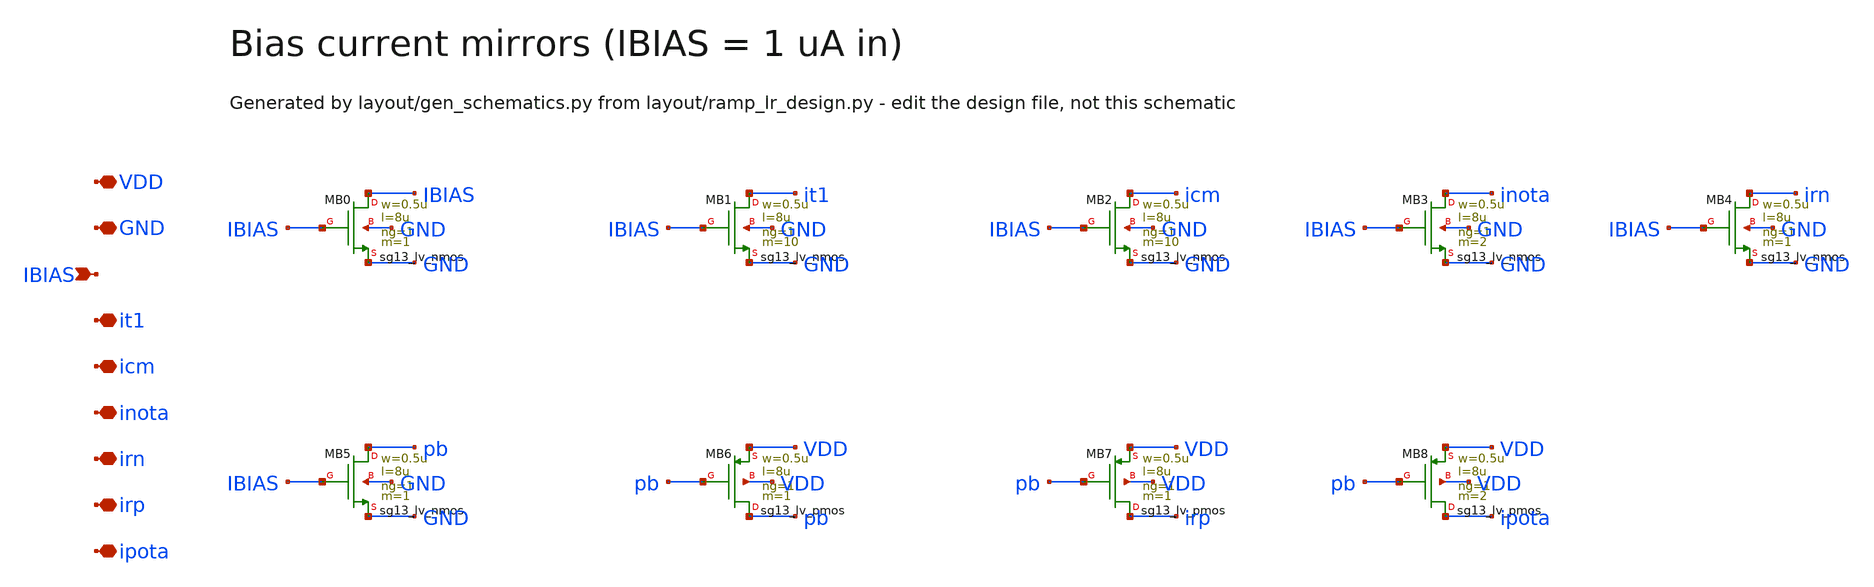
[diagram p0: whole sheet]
** sch_path: Design Files/RAMP/RAMP-LR/BIAS_LR.sch
**.subckt BIAS_LR VDD GND IBIAS it1 icm inota irn irp ipota
*.iopin VDD
*.iopin GND
*.ipin IBIAS
*.iopin it1
*.iopin icm
*.iopin inota
*.iopin irn
*.iopin irp
*.iopin ipota
XMB0 IBIAS IBIAS GND GND sg13_lv_nmos w=0.5u l=8u ng=1 m=1 mm_ok=1
XMB1 it1 IBIAS GND GND sg13_lv_nmos w=0.5u l=8u ng=1 m=10 mm_ok=1
XMB2 icm IBIAS GND GND sg13_lv_nmos w=0.5u l=8u ng=1 m=10 mm_ok=1
XMB3 inota IBIAS GND GND sg13_lv_nmos w=0.5u l=8u ng=1 m=2 mm_ok=1
XMB4 irn IBIAS GND GND sg13_lv_nmos w=0.5u l=8u ng=1 m=1 mm_ok=1
XMB5 pb IBIAS GND GND sg13_lv_nmos w=0.5u l=8u ng=1 m=1 mm_ok=1
XMB6 pb pb VDD VDD sg13_lv_pmos w=0.5u l=8u ng=1 m=1 mm_ok=1
XMB7 irp pb VDD VDD sg13_lv_pmos w=0.5u l=8u ng=1 m=1 mm_ok=1
XMB8 ipota pb VDD VDD sg13_lv_pmos w=0.5u l=8u ng=1 m=2 mm_ok=1
**.ends
.end
